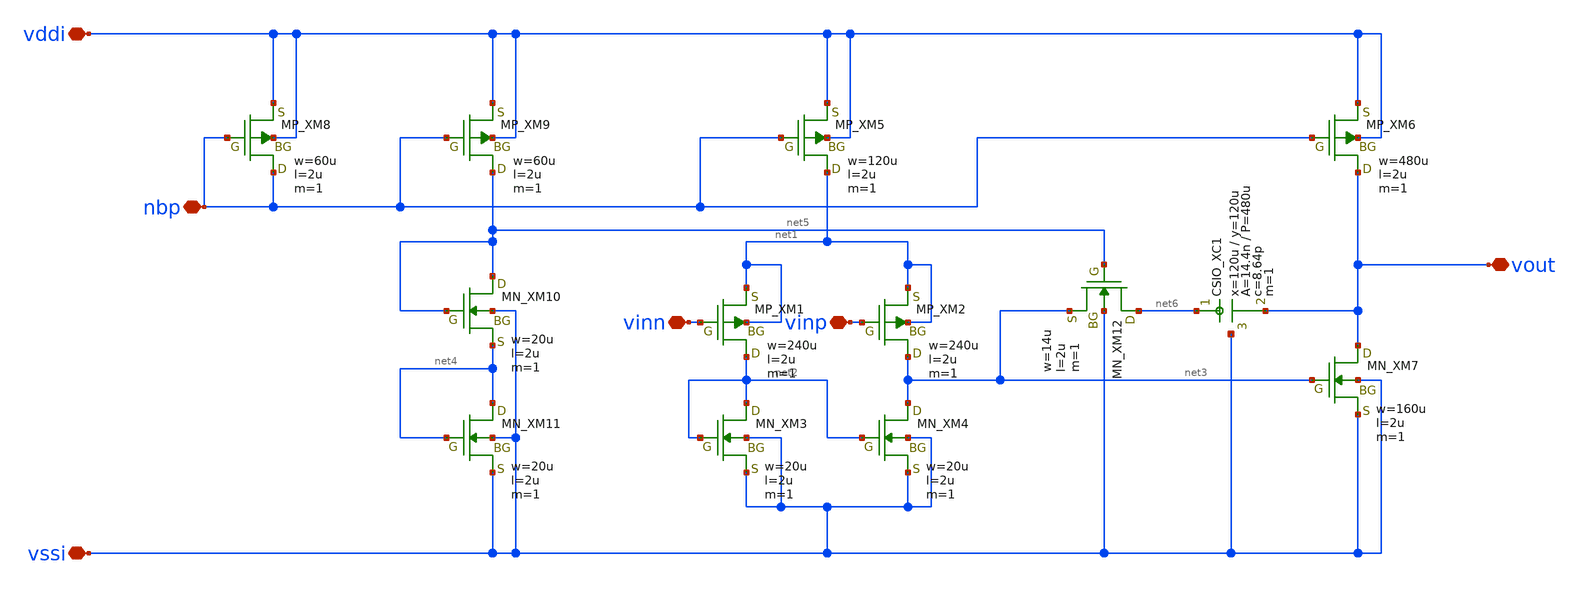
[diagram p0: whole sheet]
** sch_path: member_project/opamp/yamada/opamp_yamada.sch
**.subckt opamp_yamada vssi vddi nbp vinn vinp vout
*.iopin vssi
*.iopin vddi
*.iopin nbp
*.iopin vinn
*.iopin vinp
*.iopin vout
XXM8 nbp nbp vddi vddi PMOS w=60u l=2u nrd=0 nrs=0 m=1
XXM5 net1 nbp vddi vddi PMOS w=120u l=2u nrd=0 nrs=0 m=1
XXM1 net2 vinn net1 net1 PMOS w=240u l=2u nrd=0 nrs=0 m=1
XXM2 net3 vinp net1 net1 PMOS w=240u l=2u nrd=0 nrs=0 m=1
XXM3 net2 net2 vssi vssi NMOS w=20u l=2u nrd=0 nrs=0 m=1
XXM4 net3 net2 vssi vssi NMOS w=20u l=2u nrd=0 nrs=0 m=1
XXM6 vout nbp vddi vddi PMOS w=480u l=2u nrd=0 nrs=0 m=1
XXM7 vout net3 vssi vssi NMOS w=160u l=2u nrd=0 nrs=0 m=1
XXM9 net5 nbp vddi vddi PMOS w=60u l=2u nrd=0 nrs=0 m=1
XXM10 net5 net5 net4 vssi NMOS w=20u l=2u nrd=0 nrs=0 m=1
XXM11 net4 net4 vssi vssi NMOS w=20u l=2u nrd=0 nrs=0 m=1
XXM12 net6 net5 net3 vssi NMOS w=14u l=2u nrd=0 nrs=0 m=1
XXC1 net6 vout vssi F_CSIO c=8.64p x=120u y=120u m=1
**.ends
.end
